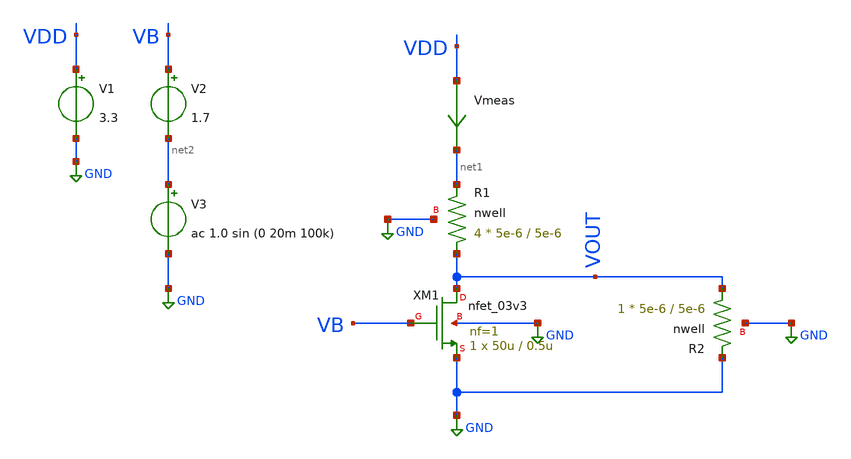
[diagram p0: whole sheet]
** sch_path: simple_amp1.sch
**.subckt simple_amp1
XM1 VOUT VB GND GND nfet_03v3 L=0.5u W=50u nf=1 ad='int((nf+1)/2) * W/nf * 0.18u' as='int((nf+2)/2) * W/nf * 0.18u'
+ pd='2*int((nf+1)/2) * (W/nf + 0.18u)' ps='2*int((nf+2)/2) * (W/nf + 0.18u)' nrd='0.18u / W' nrs='0.18u / W'
+ sa=0 sb=0 sd=0 m=1
Vmeas VDD net1 0
.save i(vmeas)
V1 VDD GND 3.3
V2 VB net2 1.7
XR1 VOUT net1 GND nwell r_width=5e-6 r_length=5e-6 m=4
XR2 VOUT GND GND nwell r_width=5e-6 r_length=5e-6 m=1
V3 net2 GND ac 1.0 sin (0 20m 100k)
**** begin user architecture code

.include $::180MCU_MODELS/design.ngspice
.lib $::180MCU_MODELS/sm141064.ngspice typical
.lib $::180MCU_MODELS/sm141064.ngspice res_typical
.lib $::180MCU_MODELS/sm141064.ngspice moscap_typical
.lib $::180MCU_MODELS/sm141064.ngspice bjt_typical
.lib $::180MCU_MODELS/sm141064.ngspice diode_typical
.lib $::180MCU_MODELS/sm141064.ngspice mimcap_typical

.control
save all
dc V2 0 3.3 0.01
plot v(VOUT) v(VB) deriv(v(VOUT))
plot i(Vmeas)
plot deriv(v(VOUT))
tran 10ns 20u
plot (1.7-v(VB)) (1.43-v(VOUT))
ac dec 20 1 50G
plot v(VOUT)
.endc

**** end user architecture code
**.ends
.GLOBAL GND
.end
